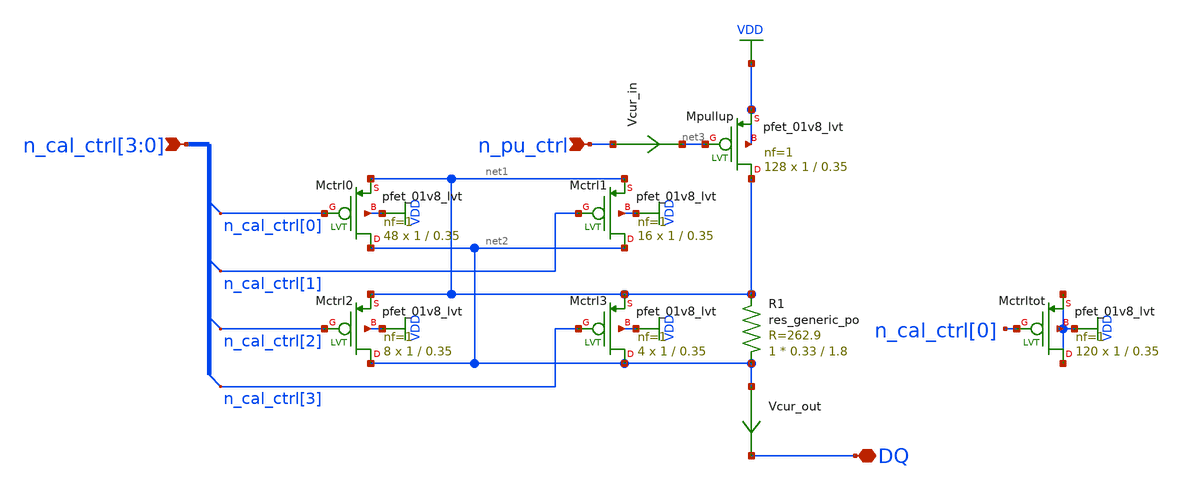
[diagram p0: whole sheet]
** sch_path: schem/p-leg.sch
* Copyright 2021 Stefan Frederik Schippers
* Licensed under the Apache License, Version 2.0 (the "License");
* you may not use this file except in compliance with the License.
* You may obtain a copy of the License at
* https://www.apache.org/licenses/LICENSE-2.0
* Unless required by applicable law or agreed to in writing, software
* distributed under the License is distributed on an "AS IS" BASIS,
* WITHOUT WARRANTIES OR CONDITIONS OF ANY KIND, either express or implied.
* See the License for the specific language governing permissions and
* limitations under the License.
**.subckt p-leg n_cal_ctrl[3],n_cal_ctrl[2],n_cal_ctrl[1],n_cal_ctrl[0] n_pu_ctrl DQ
*.ipin n_cal_ctrl[3],n_cal_ctrl[2],n_cal_ctrl[1],n_cal_ctrl[0]
*.ipin n_pu_ctrl
*.iopin DQ
XR1 net2 net1 sky130_fd_pr__res_generic_po W=0.33 L=1.8 m=1
XMpullup net1 net3 VDD VDD sky130_fd_pr__pfet_01v8_lvt L=0.35 W=1 nf=1 ad='int((nf+1)/2) * W/nf * 0.29'
+ as='int((nf+2)/2) * W/nf * 0.29' pd='2*int((nf+1)/2) * (W/nf + 0.29)' ps='2*int((nf+2)/2) * (W/nf + 0.29)'
+ nrd='0.29 / W' nrs='0.29 / W' sa=0 sb=0 sd=0 mult=128 m=128
XMctrltot VDD n_cal_ctrl[0] VDD VDD sky130_fd_pr__pfet_01v8_lvt L=0.35 W=1 nf=1 ad='int((nf+1)/2) * W/nf * 0.29'
+ as='int((nf+2)/2) * W/nf * 0.29' pd='2*int((nf+1)/2) * (W/nf + 0.29)' ps='2*int((nf+2)/2) * (W/nf + 0.29)'
+ nrd='0.29 / W' nrs='0.29 / W' sa=0 sb=0 sd=0 mult=120 m=120
XMctrl0 net2 n_cal_ctrl[0] net1 VDD sky130_fd_pr__pfet_01v8_lvt L=0.35 W=1 nf=1 ad='int((nf+1)/2) * W/nf * 0.29'
+ as='int((nf+2)/2) * W/nf * 0.29' pd='2*int((nf+1)/2) * (W/nf + 0.29)' ps='2*int((nf+2)/2) * (W/nf + 0.29)'
+ nrd='0.29 / W' nrs='0.29 / W' sa=0 sb=0 sd=0 mult=48 m=48
XMctrl1 net2 n_cal_ctrl[1] net1 VDD sky130_fd_pr__pfet_01v8_lvt L=0.35 W=1 nf=1 ad='int((nf+1)/2) * W/nf * 0.29'
+ as='int((nf+2)/2) * W/nf * 0.29' pd='2*int((nf+1)/2) * (W/nf + 0.29)' ps='2*int((nf+2)/2) * (W/nf + 0.29)'
+ nrd='0.29 / W' nrs='0.29 / W' sa=0 sb=0 sd=0 mult=16 m=16
XMctrl2 net2 n_cal_ctrl[2] net1 VDD sky130_fd_pr__pfet_01v8_lvt L=0.35 W=1 nf=1 ad='int((nf+1)/2) * W/nf * 0.29'
+ as='int((nf+2)/2) * W/nf * 0.29' pd='2*int((nf+1)/2) * (W/nf + 0.29)' ps='2*int((nf+2)/2) * (W/nf + 0.29)'
+ nrd='0.29 / W' nrs='0.29 / W' sa=0 sb=0 sd=0 mult=8 m=8
XMctrl3 net2 n_cal_ctrl[3] net1 VDD sky130_fd_pr__pfet_01v8_lvt L=0.35 W=1 nf=1 ad='int((nf+1)/2) * W/nf * 0.29'
+ as='int((nf+2)/2) * W/nf * 0.29' pd='2*int((nf+1)/2) * (W/nf + 0.29)' ps='2*int((nf+2)/2) * (W/nf + 0.29)'
+ nrd='0.29 / W' nrs='0.29 / W' sa=0 sb=0 sd=0 mult=4 m=4
Vcur_out net2 DQ 0
.save i(vcur_out)
Vcur_in n_pu_ctrl net3 0
.save i(vcur_in)
**.ends
.GLOBAL VDD
.end
